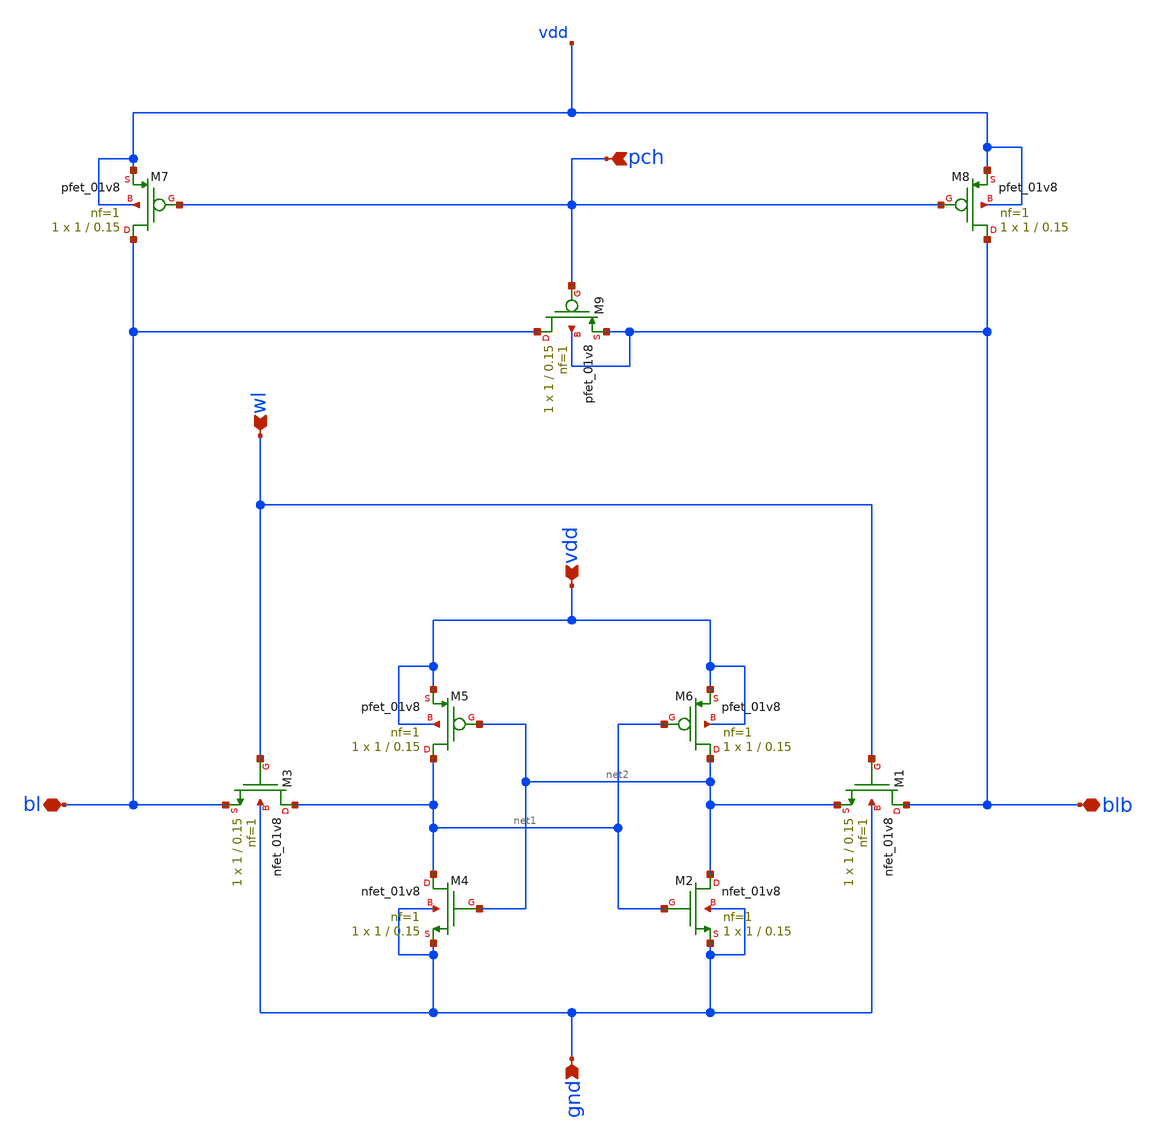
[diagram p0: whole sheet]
** sch_path: sram/sram1b_2.sch
**.subckt sram1b_2 gnd vdd wl pch blb bl
*.ipin gnd
*.ipin vdd
*.ipin wl
*.ipin pch
*.iopin blb
*.iopin bl
XM1 blb wl net2 gnd sky130_fd_pr__nfet_01v8 L=0.15 W=1 nf=1 ad='int((nf+1)/2) * W/nf * 0.29' as='int((nf+2)/2) * W/nf * 0.29'
+ pd='2*int((nf+1)/2) * (W/nf + 0.29)' ps='2*int((nf+2)/2) * (W/nf + 0.29)' nrd='0.29 / W' nrs='0.29 / W'
+ sa=0 sb=0 sd=0 mult=1 m=1
XM3 net1 wl bl gnd sky130_fd_pr__nfet_01v8 L=0.15 W=1 nf=1 ad='int((nf+1)/2) * W/nf * 0.29' as='int((nf+2)/2) * W/nf * 0.29'
+ pd='2*int((nf+1)/2) * (W/nf + 0.29)' ps='2*int((nf+2)/2) * (W/nf + 0.29)' nrd='0.29 / W' nrs='0.29 / W'
+ sa=0 sb=0 sd=0 mult=1 m=1
XM5 net1 net2 vdd vdd sky130_fd_pr__pfet_01v8 L=0.15 W=1 nf=1 ad='int((nf+1)/2) * W/nf * 0.29' as='int((nf+2)/2) * W/nf * 0.29'
+ pd='2*int((nf+1)/2) * (W/nf + 0.29)' ps='2*int((nf+2)/2) * (W/nf + 0.29)' nrd='0.29 / W' nrs='0.29 / W'
+ sa=0 sb=0 sd=0 mult=1 m=1
XM6 net2 net1 vdd vdd sky130_fd_pr__pfet_01v8 L=0.15 W=1 nf=1 ad='int((nf+1)/2) * W/nf * 0.29' as='int((nf+2)/2) * W/nf * 0.29'
+ pd='2*int((nf+1)/2) * (W/nf + 0.29)' ps='2*int((nf+2)/2) * (W/nf + 0.29)' nrd='0.29 / W' nrs='0.29 / W'
+ sa=0 sb=0 sd=0 mult=1 m=1
XM7 bl pch vdd vdd sky130_fd_pr__pfet_01v8 L=0.15 W=1 nf=1 ad='int((nf+1)/2) * W/nf * 0.29' as='int((nf+2)/2) * W/nf * 0.29'
+ pd='2*int((nf+1)/2) * (W/nf + 0.29)' ps='2*int((nf+2)/2) * (W/nf + 0.29)' nrd='0.29 / W' nrs='0.29 / W'
+ sa=0 sb=0 sd=0 mult=1 m=1
XM8 blb pch vdd vdd sky130_fd_pr__pfet_01v8 L=0.15 W=1 nf=1 ad='int((nf+1)/2) * W/nf * 0.29' as='int((nf+2)/2) * W/nf * 0.29'
+ pd='2*int((nf+1)/2) * (W/nf + 0.29)' ps='2*int((nf+2)/2) * (W/nf + 0.29)' nrd='0.29 / W' nrs='0.29 / W'
+ sa=0 sb=0 sd=0 mult=1 m=1
XM9 bl pch blb blb sky130_fd_pr__pfet_01v8 L=0.15 W=1 nf=1 ad='int((nf+1)/2) * W/nf * 0.29' as='int((nf+2)/2) * W/nf * 0.29'
+ pd='2*int((nf+1)/2) * (W/nf + 0.29)' ps='2*int((nf+2)/2) * (W/nf + 0.29)' nrd='0.29 / W' nrs='0.29 / W'
+ sa=0 sb=0 sd=0 mult=1 m=1
XM2 net2 net1 gnd gnd sky130_fd_pr__nfet_01v8 L=0.15 W=1 nf=1 ad='int((nf+1)/2) * W/nf * 0.29' as='int((nf+2)/2) * W/nf * 0.29'
+ pd='2*int((nf+1)/2) * (W/nf + 0.29)' ps='2*int((nf+2)/2) * (W/nf + 0.29)' nrd='0.29 / W' nrs='0.29 / W'
+ sa=0 sb=0 sd=0 mult=1 m=1
XM4 net1 net2 gnd gnd sky130_fd_pr__nfet_01v8 L=0.15 W=1 nf=1 ad='int((nf+1)/2) * W/nf * 0.29' as='int((nf+2)/2) * W/nf * 0.29'
+ pd='2*int((nf+1)/2) * (W/nf + 0.29)' ps='2*int((nf+2)/2) * (W/nf + 0.29)' nrd='0.29 / W' nrs='0.29 / W'
+ sa=0 sb=0 sd=0 mult=1 m=1
**.ends
.end
